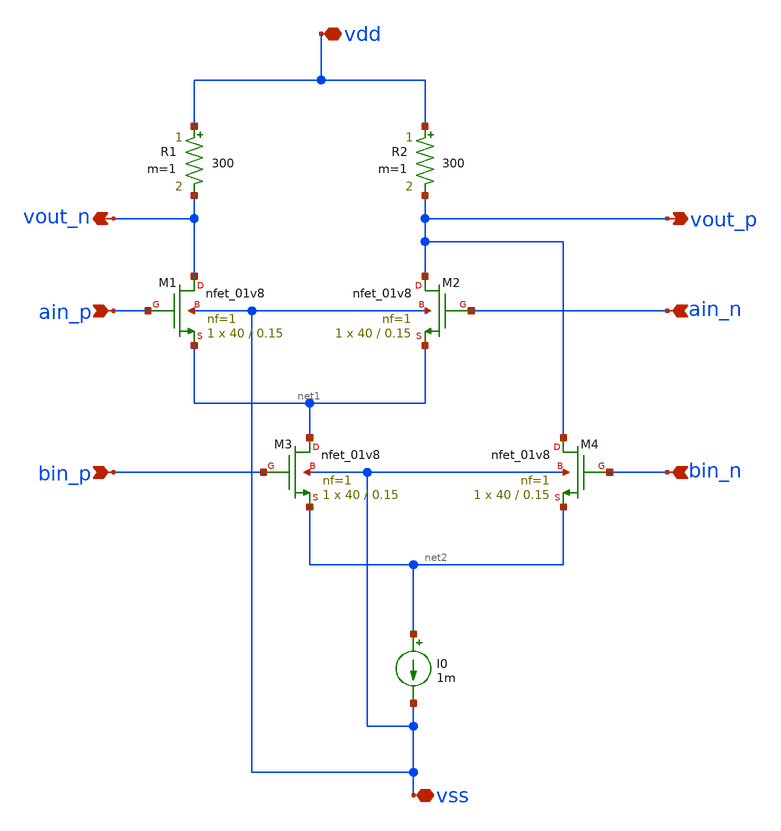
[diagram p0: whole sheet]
** sch_path: xschem/cml_and_or.sch
**.subckt cml_and_or ain_p ain_n bin_n bin_p vout_p vout_n vdd vss
*.ipin ain_p
*.ipin ain_n
*.ipin bin_n
*.ipin bin_p
*.opin vout_p
*.opin vout_n
*.iopin vdd
*.iopin vss
XM1 vout_n ain_p net1 vss sky130_fd_pr__nfet_01v8 L=0.15 W=40 nf=1 ad='int((nf+1)/2) * W/nf * 0.29' as='int((nf+2)/2) * W/nf * 0.29'
+ pd='2*int((nf+1)/2) * (W/nf + 0.29)' ps='2*int((nf+2)/2) * (W/nf + 0.29)' nrd='0.29 / W' nrs='0.29 / W'
+ sa=0 sb=0 sd=0 mult=1 m=1
XM2 vout_p ain_n net1 vss sky130_fd_pr__nfet_01v8 L=0.15 W=40 nf=1 ad='int((nf+1)/2) * W/nf * 0.29' as='int((nf+2)/2) * W/nf * 0.29'
+ pd='2*int((nf+1)/2) * (W/nf + 0.29)' ps='2*int((nf+2)/2) * (W/nf + 0.29)' nrd='0.29 / W' nrs='0.29 / W'
+ sa=0 sb=0 sd=0 mult=1 m=1
XM3 net1 bin_p net2 vss sky130_fd_pr__nfet_01v8 L=0.15 W=40 nf=1 ad='int((nf+1)/2) * W/nf * 0.29' as='int((nf+2)/2) * W/nf * 0.29'
+ pd='2*int((nf+1)/2) * (W/nf + 0.29)' ps='2*int((nf+2)/2) * (W/nf + 0.29)' nrd='0.29 / W' nrs='0.29 / W'
+ sa=0 sb=0 sd=0 mult=1 m=1
XM4 vout_p bin_n net2 vss sky130_fd_pr__nfet_01v8 L=0.15 W=40 nf=1 ad='int((nf+1)/2) * W/nf * 0.29' as='int((nf+2)/2) * W/nf * 0.29'
+ pd='2*int((nf+1)/2) * (W/nf + 0.29)' ps='2*int((nf+2)/2) * (W/nf + 0.29)' nrd='0.29 / W' nrs='0.29 / W'
+ sa=0 sb=0 sd=0 mult=1 m=1
R1 vdd vout_n 300 m=1
R2 vdd vout_p 300 m=1
I0 net2 vss 1m
**.ends
.end
